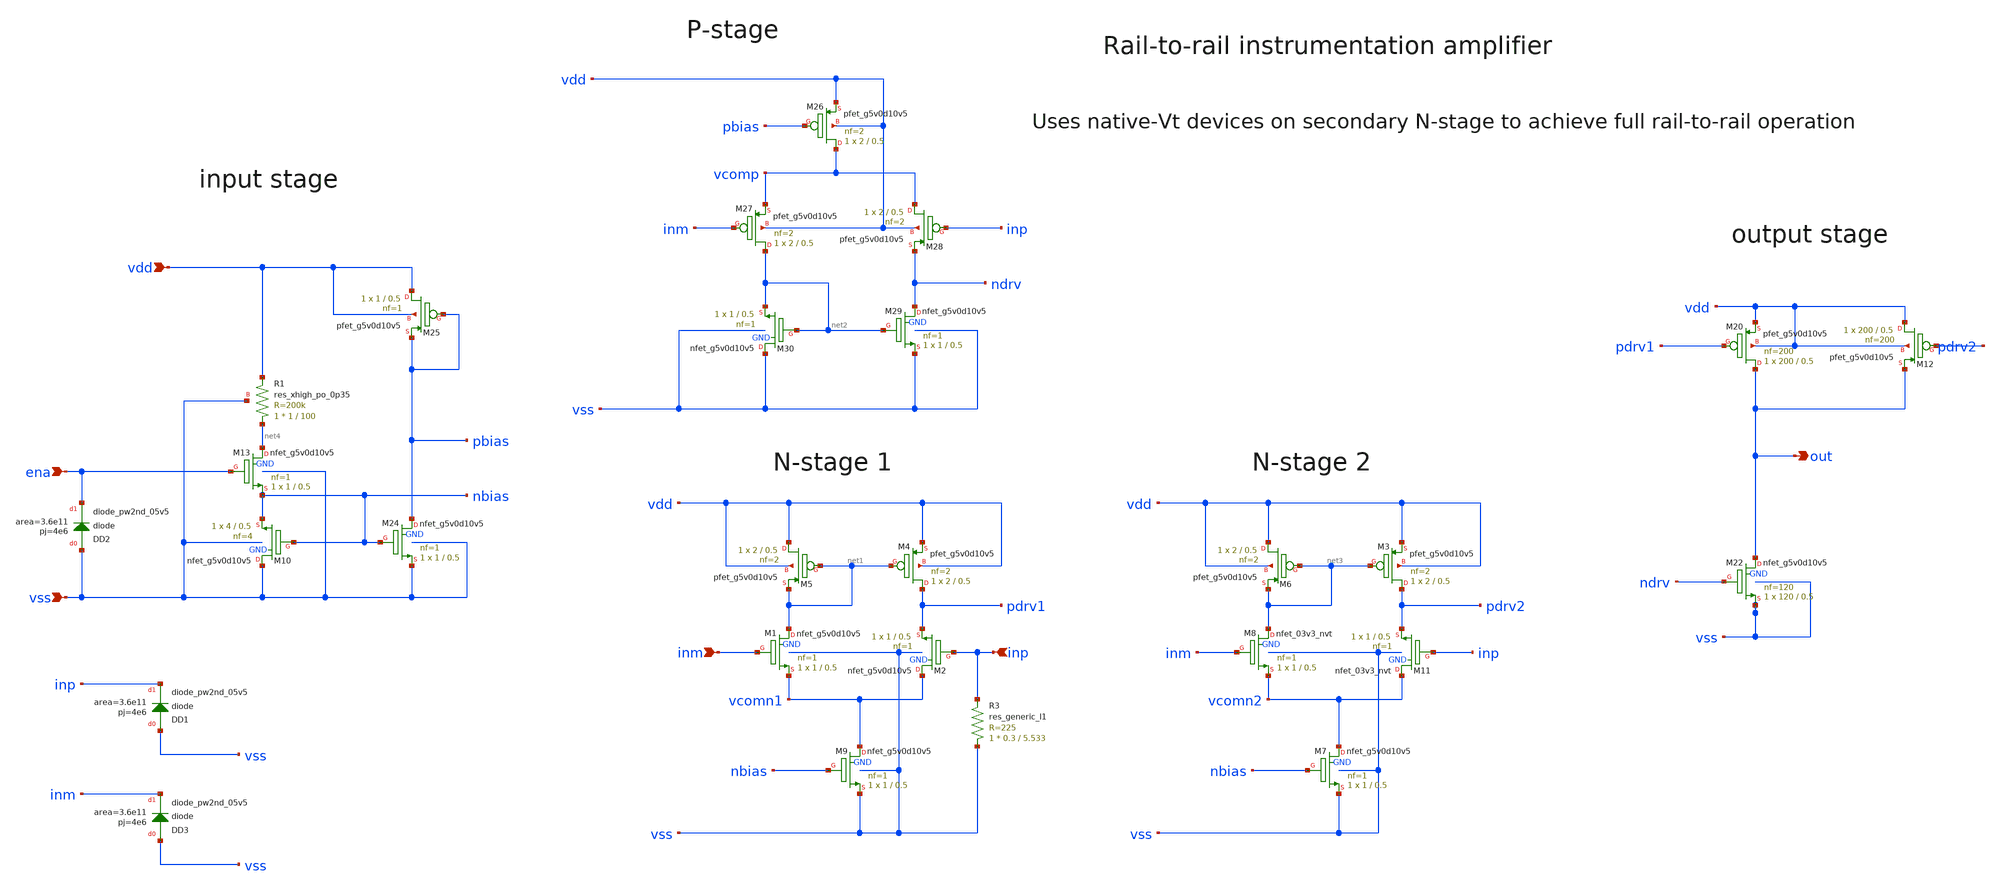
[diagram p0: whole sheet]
** sch_path: xschem/analog_desing/Buffer/sky130_ef_ip__opamp_withRin.sch
**.subckt sky130_ef_ip__opamp_withRin vdd vss out inm inp ena
*.ipin vdd
*.ipin vss
*.opin out
*.ipin inm
*.ipin inp
*.ipin ena
XM4 pdrv1 net1 vdd vdd sky130_fd_pr__pfet_g5v0d10v5 L=0.5 W=2 nf=2 ad='int((nf+1)/2) * W/nf * 0.29' as='int((nf+2)/2) * W/nf * 0.29'
+ pd='2*int((nf+1)/2) * (W/nf + 0.29)' ps='2*int((nf+2)/2) * (W/nf + 0.29)' nrd='0.29 / W' nrs='0.29 / W'
+ sa=0 sb=0 sd=0 mult=1 m=1
XM5 vdd net1 net1 vdd sky130_fd_pr__pfet_g5v0d10v5 L=0.5 W=2 nf=2 ad='int((nf+1)/2) * W/nf * 0.29' as='int((nf+2)/2) * W/nf * 0.29'
+ pd='2*int((nf+1)/2) * (W/nf + 0.29)' ps='2*int((nf+2)/2) * (W/nf + 0.29)' nrd='0.29 / W' nrs='0.29 / W'
+ sa=0 sb=0 sd=0 mult=1 m=1
XM9 vcomn1 nbias vss GND sky130_fd_pr__nfet_g5v0d10v5 L=0.5 W=1 nf=1 ad='int((nf+1)/2) * W/nf * 0.29'
+ as='int((nf+2)/2) * W/nf * 0.29' pd='2*int((nf+1)/2) * (W/nf + 0.29)' ps='2*int((nf+2)/2) * (W/nf + 0.29)'
+ nrd='0.29 / W' nrs='0.29 / W' sa=0 sb=0 sd=0 mult=1 m=1
XM10 vss nbias nbias GND sky130_fd_pr__nfet_g5v0d10v5 L=0.5 W=4 nf=4 ad='int((nf+1)/2) * W/nf * 0.29'
+ as='int((nf+2)/2) * W/nf * 0.29' pd='2*int((nf+1)/2) * (W/nf + 0.29)' ps='2*int((nf+2)/2) * (W/nf + 0.29)'
+ nrd='0.29 / W' nrs='0.29 / W' sa=0 sb=0 sd=0 mult=1 m=1
XR1 net4 vdd vss sky130_fd_pr__res_xhigh_po_0p35 W=1 L=100 mult=1 m=1
XM20 out pdrv1 vdd vdd sky130_fd_pr__pfet_g5v0d10v5 L=0.5 W=200 nf=200 ad='int((nf+1)/2) * W/nf * 0.29'
+ as='int((nf+2)/2) * W/nf * 0.29' pd='2*int((nf+1)/2) * (W/nf + 0.29)' ps='2*int((nf+2)/2) * (W/nf + 0.29)'
+ nrd='0.29 / W' nrs='0.29 / W' sa=0 sb=0 sd=0 mult=1 m=1
XM22 out ndrv vss GND sky130_fd_pr__nfet_g5v0d10v5 L=0.5 W=120 nf=120 ad='int((nf+1)/2) * W/nf * 0.29'
+ as='int((nf+2)/2) * W/nf * 0.29' pd='2*int((nf+1)/2) * (W/nf + 0.29)' ps='2*int((nf+2)/2) * (W/nf + 0.29)'
+ nrd='0.29 / W' nrs='0.29 / W' sa=0 sb=0 sd=0 mult=1 m=1
XM24 pbias nbias vss GND sky130_fd_pr__nfet_g5v0d10v5 L=0.5 W=1 nf=1 ad='int((nf+1)/2) * W/nf * 0.29'
+ as='int((nf+2)/2) * W/nf * 0.29' pd='2*int((nf+1)/2) * (W/nf + 0.29)' ps='2*int((nf+2)/2) * (W/nf + 0.29)'
+ nrd='0.29 / W' nrs='0.29 / W' sa=0 sb=0 sd=0 mult=1 m=1
XM25 vdd pbias pbias vdd sky130_fd_pr__pfet_g5v0d10v5 L=0.5 W=1 nf=1 ad='int((nf+1)/2) * W/nf * 0.29'
+ as='int((nf+2)/2) * W/nf * 0.29' pd='2*int((nf+1)/2) * (W/nf + 0.29)' ps='2*int((nf+2)/2) * (W/nf + 0.29)'
+ nrd='0.29 / W' nrs='0.29 / W' sa=0 sb=0 sd=0 mult=1 m=1
XM26 vcomp pbias vdd vdd sky130_fd_pr__pfet_g5v0d10v5 L=0.5 W=2 nf=2 ad='int((nf+1)/2) * W/nf * 0.29'
+ as='int((nf+2)/2) * W/nf * 0.29' pd='2*int((nf+1)/2) * (W/nf + 0.29)' ps='2*int((nf+2)/2) * (W/nf + 0.29)'
+ nrd='0.29 / W' nrs='0.29 / W' sa=0 sb=0 sd=0 mult=1 m=1
XM27 net2 inm vcomp vdd sky130_fd_pr__pfet_g5v0d10v5 L=0.5 W=2 nf=2 ad='int((nf+1)/2) * W/nf * 0.29'
+ as='int((nf+2)/2) * W/nf * 0.29' pd='2*int((nf+1)/2) * (W/nf + 0.29)' ps='2*int((nf+2)/2) * (W/nf + 0.29)'
+ nrd='0.29 / W' nrs='0.29 / W' sa=0 sb=0 sd=0 mult=1 m=1
XM28 vcomp inp ndrv vdd sky130_fd_pr__pfet_g5v0d10v5 L=0.5 W=2 nf=2 ad='int((nf+1)/2) * W/nf * 0.29'
+ as='int((nf+2)/2) * W/nf * 0.29' pd='2*int((nf+1)/2) * (W/nf + 0.29)' ps='2*int((nf+2)/2) * (W/nf + 0.29)'
+ nrd='0.29 / W' nrs='0.29 / W' sa=0 sb=0 sd=0 mult=1 m=1
XM29 ndrv net2 vss GND sky130_fd_pr__nfet_g5v0d10v5 L=0.5 W=1 nf=1 ad='int((nf+1)/2) * W/nf * 0.29' as='int((nf+2)/2) * W/nf * 0.29'
+ pd='2*int((nf+1)/2) * (W/nf + 0.29)' ps='2*int((nf+2)/2) * (W/nf + 0.29)' nrd='0.29 / W' nrs='0.29 / W'
+ sa=0 sb=0 sd=0 mult=1 m=1
XM30 vss net2 net2 GND sky130_fd_pr__nfet_g5v0d10v5 L=0.5 W=1 nf=1 ad='int((nf+1)/2) * W/nf * 0.29' as='int((nf+2)/2) * W/nf * 0.29'
+ pd='2*int((nf+1)/2) * (W/nf + 0.29)' ps='2*int((nf+2)/2) * (W/nf + 0.29)' nrd='0.29 / W' nrs='0.29 / W'
+ sa=0 sb=0 sd=0 mult=1 m=1
XM1 net1 inm vcomn1 GND sky130_fd_pr__nfet_g5v0d10v5 L=0.5 W=1 nf=1 ad='int((nf+1)/2) * W/nf * 0.29'
+ as='int((nf+2)/2) * W/nf * 0.29' pd='2*int((nf+1)/2) * (W/nf + 0.29)' ps='2*int((nf+2)/2) * (W/nf + 0.29)'
+ nrd='0.29 / W' nrs='0.29 / W' sa=0 sb=0 sd=0 mult=1 m=1
XM2 vcomn1 inp pdrv1 GND sky130_fd_pr__nfet_g5v0d10v5 L=0.5 W=1 nf=1 ad='int((nf+1)/2) * W/nf * 0.29'
+ as='int((nf+2)/2) * W/nf * 0.29' pd='2*int((nf+1)/2) * (W/nf + 0.29)' ps='2*int((nf+2)/2) * (W/nf + 0.29)'
+ nrd='0.29 / W' nrs='0.29 / W' sa=0 sb=0 sd=0 mult=1 m=1
XM3 pdrv2 net3 vdd vdd sky130_fd_pr__pfet_g5v0d10v5 L=0.5 W=2 nf=2 ad='int((nf+1)/2) * W/nf * 0.29' as='int((nf+2)/2) * W/nf * 0.29'
+ pd='2*int((nf+1)/2) * (W/nf + 0.29)' ps='2*int((nf+2)/2) * (W/nf + 0.29)' nrd='0.29 / W' nrs='0.29 / W'
+ sa=0 sb=0 sd=0 mult=1 m=1
XM6 vdd net3 net3 vdd sky130_fd_pr__pfet_g5v0d10v5 L=0.5 W=2 nf=2 ad='int((nf+1)/2) * W/nf * 0.29' as='int((nf+2)/2) * W/nf * 0.29'
+ pd='2*int((nf+1)/2) * (W/nf + 0.29)' ps='2*int((nf+2)/2) * (W/nf + 0.29)' nrd='0.29 / W' nrs='0.29 / W'
+ sa=0 sb=0 sd=0 mult=1 m=1
XM7 vcomn2 nbias vss GND sky130_fd_pr__nfet_g5v0d10v5 L=0.5 W=1 nf=1 ad='int((nf+1)/2) * W/nf * 0.29'
+ as='int((nf+2)/2) * W/nf * 0.29' pd='2*int((nf+1)/2) * (W/nf + 0.29)' ps='2*int((nf+2)/2) * (W/nf + 0.29)'
+ nrd='0.29 / W' nrs='0.29 / W' sa=0 sb=0 sd=0 mult=1 m=1
XM8 net3 inm vcomn2 GND sky130_fd_pr__nfet_03v3_nvt L=0.5 W=1 nf=1 ad='int((nf+1)/2) * W/nf * 0.29' as='int((nf+2)/2) * W/nf * 0.29'
+ pd='2*int((nf+1)/2) * (W/nf + 0.29)' ps='2*int((nf+2)/2) * (W/nf + 0.29)' nrd='0.29 / W' nrs='0.29 / W'
+ sa=0 sb=0 sd=0 mult=1 m=1
XM11 vcomn2 inp pdrv2 GND sky130_fd_pr__nfet_03v3_nvt L=0.5 W=1 nf=1 ad='int((nf+1)/2) * W/nf * 0.29'
+ as='int((nf+2)/2) * W/nf * 0.29' pd='2*int((nf+1)/2) * (W/nf + 0.29)' ps='2*int((nf+2)/2) * (W/nf + 0.29)'
+ nrd='0.29 / W' nrs='0.29 / W' sa=0 sb=0 sd=0 mult=1 m=1
XM12 vdd pdrv2 out vdd sky130_fd_pr__pfet_g5v0d10v5 L=0.5 W=200 nf=200 ad='int((nf+1)/2) * W/nf * 0.29'
+ as='int((nf+2)/2) * W/nf * 0.29' pd='2*int((nf+1)/2) * (W/nf + 0.29)' ps='2*int((nf+2)/2) * (W/nf + 0.29)'
+ nrd='0.29 / W' nrs='0.29 / W' sa=0 sb=0 sd=0 mult=1 m=1
XDD1 vss inp sky130_fd_pr__diode_pw2nd_05v5 area=3.6e11 pj=4e6
XM13 net4 ena nbias GND sky130_fd_pr__nfet_g5v0d10v5 L=0.5 W=1 nf=1 ad='int((nf+1)/2) * W/nf * 0.29'
+ as='int((nf+2)/2) * W/nf * 0.29' pd='2*int((nf+1)/2) * (W/nf + 0.29)' ps='2*int((nf+2)/2) * (W/nf + 0.29)'
+ nrd='0.29 / W' nrs='0.29 / W' sa=0 sb=0 sd=0 mult=1 m=1
XDD2 vss ena sky130_fd_pr__diode_pw2nd_05v5 area=3.6e11 pj=4e6
XDD3 vss inm sky130_fd_pr__diode_pw2nd_05v5 area=3.6e11 pj=4e6
R3 vss inp sky130_fd_pr__res_generic_l1 W=0.3 L=5.533 m=1
**.ends
.end
